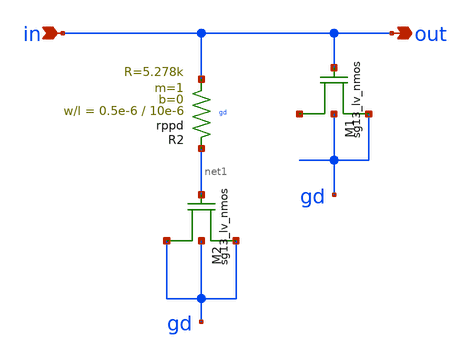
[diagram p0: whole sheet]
** sch_path: schematics/misc/RC_filter.sch
**.subckt RC_filter in out
*.ipin in
*.opin out
XM1 gd in net2 gd sg13_lv_nmos w=10u l=10u ng=1 m=5
XR2 net1 in gd rppd w=0.5e-6 l=10e-6 m=1 b=0 mm_ok=1
XM2 gd net1 gd gd sg13_lv_nmos w=10u l=10u ng=1 m=5
**.ends
.end
